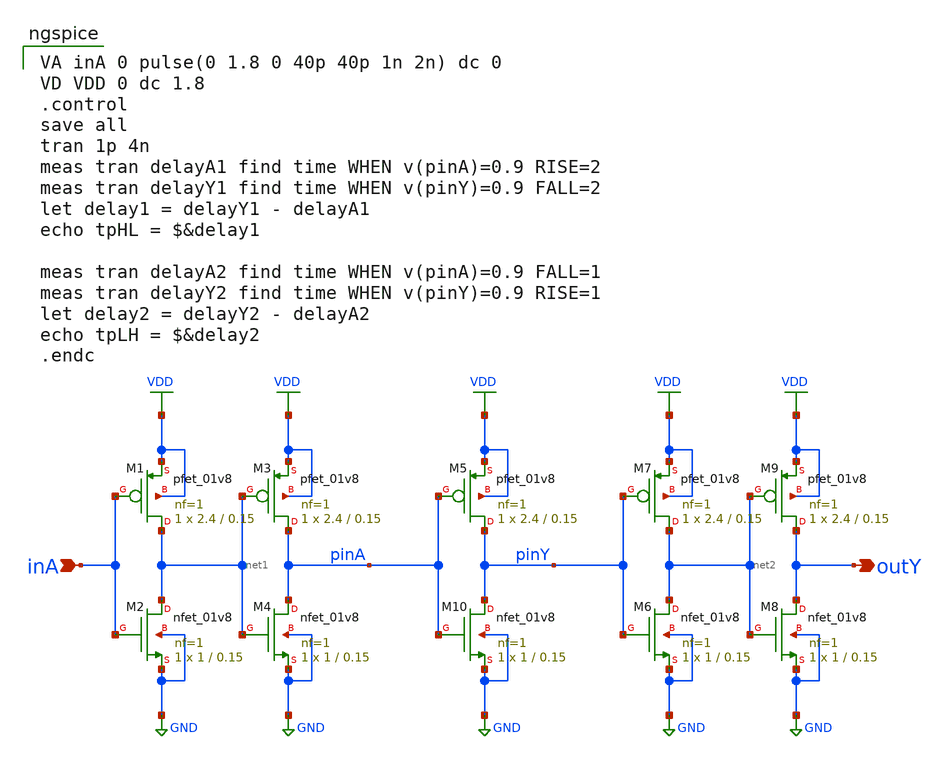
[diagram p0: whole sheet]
** sch_path: inv_meas.sch
**.subckt inv_meas inA outY
*.ipin inA
*.opin outY
XM1 net1 inA VDD VDD sky130_fd_pr__pfet_01v8 L=0.15 W=2.4 nf=1 ad='int((nf+1)/2) * W/nf * 0.29' as='int((nf+2)/2) * W/nf * 0.29'
+ pd='2*int((nf+1)/2) * (W/nf + 0.29)' ps='2*int((nf+2)/2) * (W/nf + 0.29)' nrd='0.29 / W' nrs='0.29 / W'
+ sa=0 sb=0 sd=0 mult=1 m=1
XM2 net1 inA GND GND sky130_fd_pr__nfet_01v8 L=0.15 W=1 nf=1 ad='int((nf+1)/2) * W/nf * 0.29' as='int((nf+2)/2) * W/nf * 0.29'
+ pd='2*int((nf+1)/2) * (W/nf + 0.29)' ps='2*int((nf+2)/2) * (W/nf + 0.29)' nrd='0.29 / W' nrs='0.29 / W'
+ sa=0 sb=0 sd=0 mult=1 m=1
XM4 pinA net1 GND GND sky130_fd_pr__nfet_01v8 L=0.15 W=1 nf=1 ad='int((nf+1)/2) * W/nf * 0.29' as='int((nf+2)/2) * W/nf * 0.29'
+ pd='2*int((nf+1)/2) * (W/nf + 0.29)' ps='2*int((nf+2)/2) * (W/nf + 0.29)' nrd='0.29 / W' nrs='0.29 / W'
+ sa=0 sb=0 sd=0 mult=1 m=1
XM6 net2 pinY GND GND sky130_fd_pr__nfet_01v8 L=0.15 W=1 nf=1 ad='int((nf+1)/2) * W/nf * 0.29' as='int((nf+2)/2) * W/nf * 0.29'
+ pd='2*int((nf+1)/2) * (W/nf + 0.29)' ps='2*int((nf+2)/2) * (W/nf + 0.29)' nrd='0.29 / W' nrs='0.29 / W'
+ sa=0 sb=0 sd=0 mult=1 m=1
XM8 outY net2 GND GND sky130_fd_pr__nfet_01v8 L=0.15 W=1 nf=1 ad='int((nf+1)/2) * W/nf * 0.29' as='int((nf+2)/2) * W/nf * 0.29'
+ pd='2*int((nf+1)/2) * (W/nf + 0.29)' ps='2*int((nf+2)/2) * (W/nf + 0.29)' nrd='0.29 / W' nrs='0.29 / W'
+ sa=0 sb=0 sd=0 mult=1 m=1
XM10 pinY pinA GND GND sky130_fd_pr__nfet_01v8 L=0.15 W=1 nf=1 ad='int((nf+1)/2) * W/nf * 0.29' as='int((nf+2)/2) * W/nf * 0.29'
+ pd='2*int((nf+1)/2) * (W/nf + 0.29)' ps='2*int((nf+2)/2) * (W/nf + 0.29)' nrd='0.29 / W' nrs='0.29 / W'
+ sa=0 sb=0 sd=0 mult=1 m=1
XM3 pinA net1 VDD VDD sky130_fd_pr__pfet_01v8 L=0.15 W=2.4 nf=1 ad='int((nf+1)/2) * W/nf * 0.29' as='int((nf+2)/2) * W/nf * 0.29'
+ pd='2*int((nf+1)/2) * (W/nf + 0.29)' ps='2*int((nf+2)/2) * (W/nf + 0.29)' nrd='0.29 / W' nrs='0.29 / W'
+ sa=0 sb=0 sd=0 mult=1 m=1
XM5 pinY pinA VDD VDD sky130_fd_pr__pfet_01v8 L=0.15 W=2.4 nf=1 ad='int((nf+1)/2) * W/nf * 0.29' as='int((nf+2)/2) * W/nf * 0.29'
+ pd='2*int((nf+1)/2) * (W/nf + 0.29)' ps='2*int((nf+2)/2) * (W/nf + 0.29)' nrd='0.29 / W' nrs='0.29 / W'
+ sa=0 sb=0 sd=0 mult=1 m=1
XM7 net2 pinY VDD VDD sky130_fd_pr__pfet_01v8 L=0.15 W=2.4 nf=1 ad='int((nf+1)/2) * W/nf * 0.29' as='int((nf+2)/2) * W/nf * 0.29'
+ pd='2*int((nf+1)/2) * (W/nf + 0.29)' ps='2*int((nf+2)/2) * (W/nf + 0.29)' nrd='0.29 / W' nrs='0.29 / W'
+ sa=0 sb=0 sd=0 mult=1 m=1
XM9 outY net2 VDD VDD sky130_fd_pr__pfet_01v8 L=0.15 W=2.4 nf=1 ad='int((nf+1)/2) * W/nf * 0.29' as='int((nf+2)/2) * W/nf * 0.29'
+ pd='2*int((nf+1)/2) * (W/nf + 0.29)' ps='2*int((nf+2)/2) * (W/nf + 0.29)' nrd='0.29 / W' nrs='0.29 / W'
+ sa=0 sb=0 sd=0 mult=1 m=1
**** begin user architecture code

VA inA 0 pulse(0 1.8 0 40p 40p 1n 2n) dc 0
VD VDD 0 dc 1.8
.control
save all
tran 1p 4n
meas tran delayA1 find time WHEN v(pinA)=0.9 RISE=2
meas tran delayY1 find time WHEN v(pinY)=0.9 FALL=2
let delay1 = delayY1 - delayA1
echo tpHL = $&delay1

meas tran delayA2 find time WHEN v(pinA)=0.9 FALL=1
meas tran delayY2 find time WHEN v(pinY)=0.9 RISE=1
let delay2 = delayY2 - delayA2
echo tpLH = $&delay2
.endc

 .param mc_mm_switch=0
.param mc_pr_switch=0
.include $::SKYWATER_MODELS/corners/tt.spice
.include $::SKYWATER_MODELS/r+c/res_typical__cap_typical.spice
.include $::SKYWATER_MODELS/r+c/res_typical__cap_typical__lin.spice
.include $::SKYWATER_MODELS/corners/tt/specialized_cells.spice
.include $::SKYWATER_STDCELLS/sky130_fd_sc_hd.spice

**** end user architecture code
**.ends
.GLOBAL GND
.GLOBAL VDD
.end
